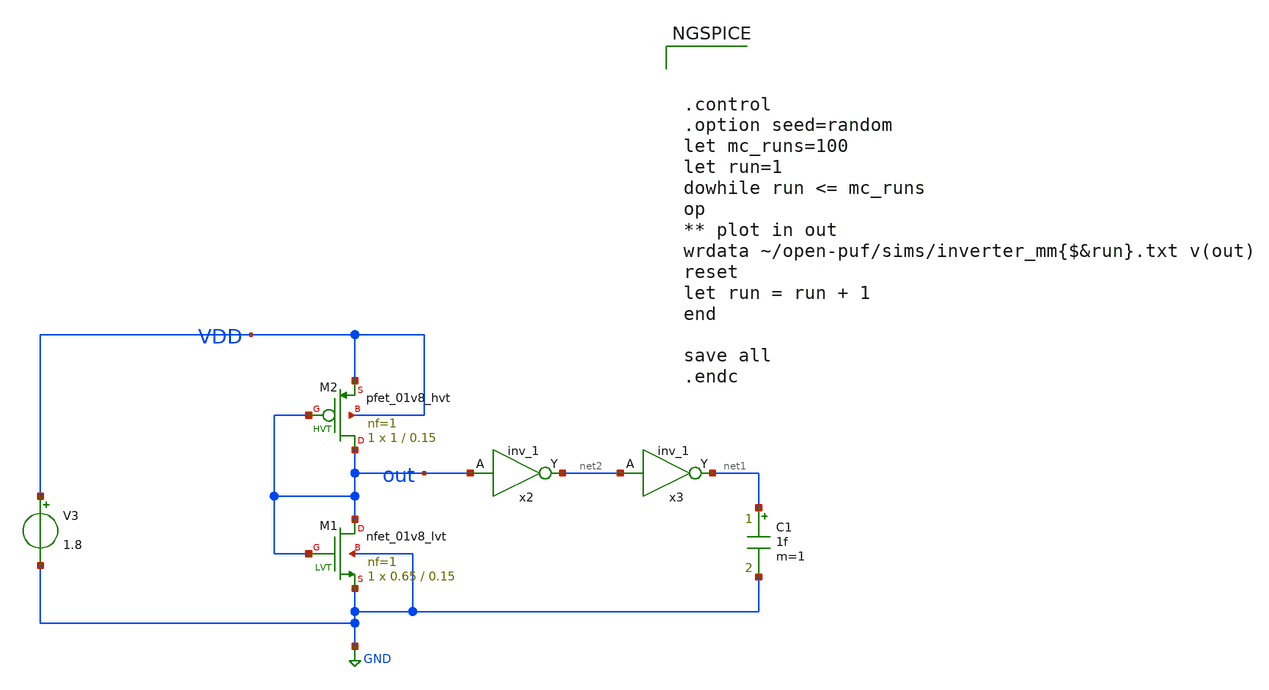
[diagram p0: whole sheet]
** sch_path: design/inverter_mm.sch
**.subckt inverter_mm
C1 net1 GND 1f m=1
XM1 out out GND GND sky130_fd_pr__nfet_01v8_lvt L=0.15 W=0.65 nf=1 ad='int((nf+1)/2) * W/nf * 0.29' as='int((nf+2)/2) * W/nf * 0.29'
+ pd='2*int((nf+1)/2) * (W/nf + 0.29)' ps='2*int((nf+2)/2) * (W/nf + 0.29)' nrd='0.29 / W' nrs='0.29 / W'
+ sa=0 sb=0 sd=0 mult=1 m=1
XM2 out out VDD VDD sky130_fd_pr__pfet_01v8_hvt L=0.15 W=1 nf=1 ad='int((nf+1)/2) * W/nf * 0.29' as='int((nf+2)/2) * W/nf * 0.29'
+ pd='2*int((nf+1)/2) * (W/nf + 0.29)' ps='2*int((nf+2)/2) * (W/nf + 0.29)' nrd='0.29 / W' nrs='0.29 / W'
+ sa=0 sb=0 sd=0 mult=1 m=1
V3 VDD GND 1.8
x2 out 0 0 VDD VDD net2 sky130_fd_sc_hd__inv_1
x3 net2 0 0 VDD VDD net1 sky130_fd_sc_hd__inv_1
**** begin user architecture code

** opencircuitdesign pdks install
.lib $::SKYWATER_MODELS/sky130.lib.spice tt_mm
.include $::SKYWATER_STDCELLS/sky130_fd_sc_hd.spice





.control
.option seed=random
let mc_runs=100
let run=1
dowhile run <= mc_runs
op
** plot in out
wrdata ~/open-puf/sims/inverter_mm{$&run}.txt v(out)
reset
let run = run + 1
end

save all
.endc


**** end user architecture code
**.ends
.GLOBAL GND
.end
